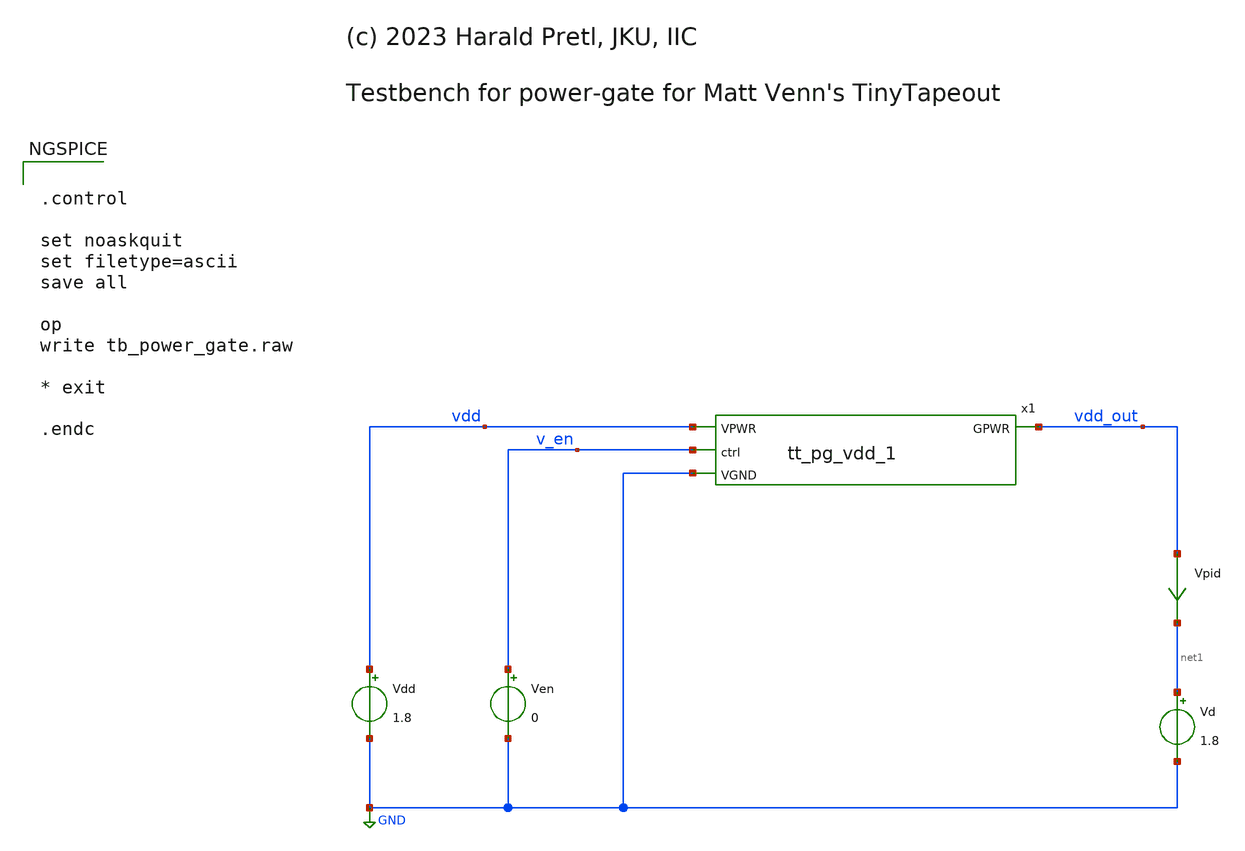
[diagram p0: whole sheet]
** sch_path: tt_pg_vdd_1/work/tb_tt_pg_vdd_1.sch
* (c) 2023 Harald Pretl, JKU, IIC
**.subckt tb_tt_pg_vdd_1
Ven v_en GND 0
Vdd vdd GND 1.8
Vpid vdd_out net1 0
.save i(vpid)
Vd net1 GND 1.8
x1 vdd vdd_out v_en GND tt_pg_vdd_1
**** begin user architecture code
 ** manual skywater pdks install (with patches applied)
* .lib $::SKYWATER_MODELS/models/sky130.lib.spice tt

** opencircuitdesign pdks install
.lib $::SKYWATER_MODELS/sky130.lib.spice.tt.red tt

.param mc_mm_switch=0
.param mc_pr_switch=0



.control

set noaskquit
set filetype=ascii
save all

op
write tb_power_gate.raw

* exit

.endc


**** end user architecture code
**.ends
.GLOBAL GND
.end
